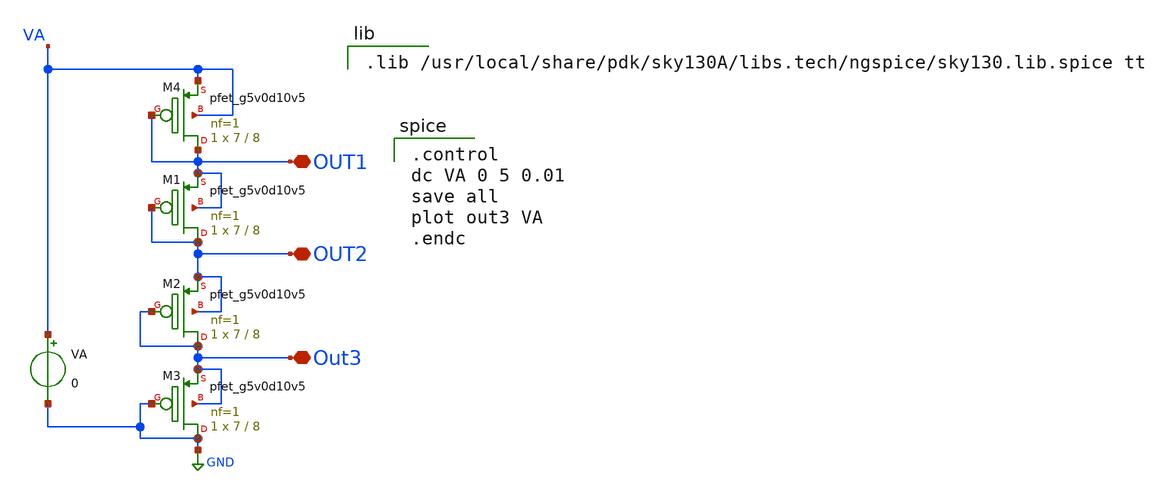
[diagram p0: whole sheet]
** sch_path: xschem/untitled.sch
**.subckt untitled OUT1 OUT2 Out3
*.iopin OUT1
*.iopin OUT2
*.iopin Out3
VA VA GND 0
XM1 OUT2 OUT2 OUT1 OUT1 sky130_fd_pr__pfet_g5v0d10v5 L=8 W=7 nf=1 ad='int((nf+1)/2) * W/nf * 0.29' as='int((nf+2)/2) * W/nf * 0.29'
+ pd='2*int((nf+1)/2) * (W/nf + 0.29)' ps='2*int((nf+2)/2) * (W/nf + 0.29)' nrd='0.29 / W' nrs='0.29 / W'
+ sa=0 sb=0 sd=0 mult=1 m=1
XM2 Out3 Out3 OUT2 OUT2 sky130_fd_pr__pfet_g5v0d10v5 L=8 W=7 nf=1 ad='int((nf+1)/2) * W/nf * 0.29' as='int((nf+2)/2) * W/nf * 0.29'
+ pd='2*int((nf+1)/2) * (W/nf + 0.29)' ps='2*int((nf+2)/2) * (W/nf + 0.29)' nrd='0.29 / W' nrs='0.29 / W'
+ sa=0 sb=0 sd=0 mult=1 m=1
XM3 GND GND Out3 Out3 sky130_fd_pr__pfet_g5v0d10v5 L=8 W=7 nf=1 ad='int((nf+1)/2) * W/nf * 0.29' as='int((nf+2)/2) * W/nf * 0.29'
+ pd='2*int((nf+1)/2) * (W/nf + 0.29)' ps='2*int((nf+2)/2) * (W/nf + 0.29)' nrd='0.29 / W' nrs='0.29 / W'
+ sa=0 sb=0 sd=0 mult=1 m=1
XM4 OUT1 OUT1 VA VA sky130_fd_pr__pfet_g5v0d10v5 L=8 W=7 nf=1 ad='int((nf+1)/2) * W/nf * 0.29' as='int((nf+2)/2) * W/nf * 0.29'
+ pd='2*int((nf+1)/2) * (W/nf + 0.29)' ps='2*int((nf+2)/2) * (W/nf + 0.29)' nrd='0.29 / W' nrs='0.29 / W'
+ sa=0 sb=0 sd=0 mult=1 m=1
**** begin user architecture code

.control
dc VA 0 5 0.01
save all
plot out3 VA
.endc


.lib /usr/local/share/pdk/sky130A/libs.tech/ngspice/sky130.lib.spice tt

**** end user architecture code
**.ends
.GLOBAL GND
.end
